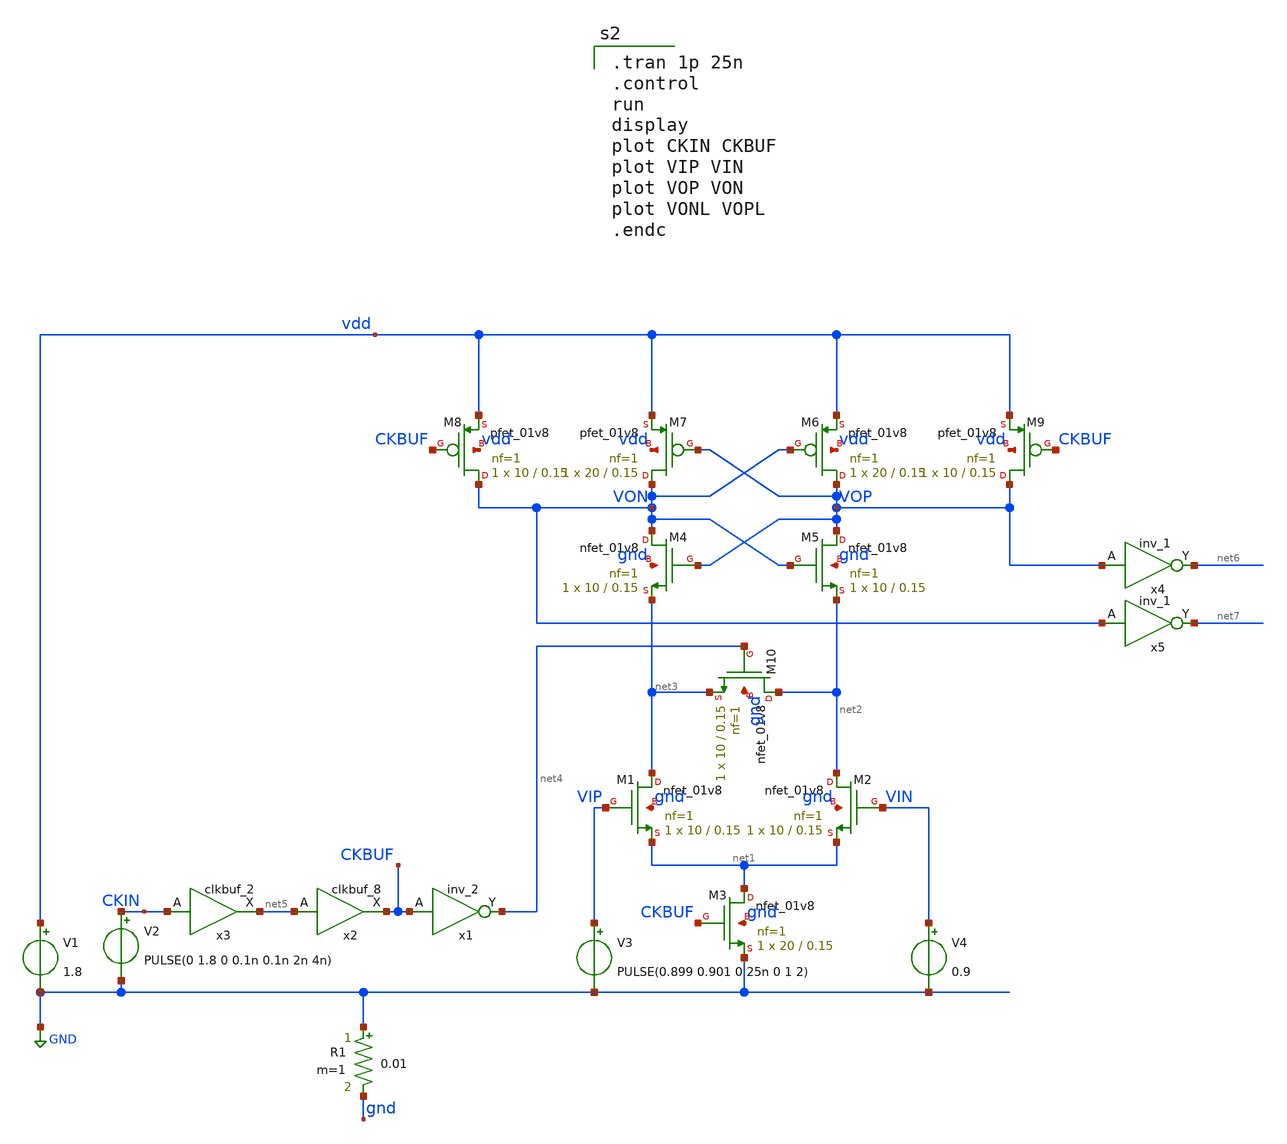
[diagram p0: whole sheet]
** sch_path: xschem/adc_strongarm.sch
**.subckt adc_strongarm
XM1 net3 VIP net1 gnd sky130_fd_pr__nfet_01v8 L=0.15 W=10 nf=1 ad='int((nf+1)/2) * W/nf * 0.29' as='int((nf+2)/2) * W/nf * 0.29'
+ pd='2*int((nf+1)/2) * (W/nf + 0.29)' ps='2*int((nf+2)/2) * (W/nf + 0.29)' nrd='0.29 / W' nrs='0.29 / W'
+ sa=0 sb=0 sd=0 mult=1 m=1
XM2 net2 VIN net1 gnd sky130_fd_pr__nfet_01v8 L=0.15 W=10 nf=1 ad='int((nf+1)/2) * W/nf * 0.29' as='int((nf+2)/2) * W/nf * 0.29'
+ pd='2*int((nf+1)/2) * (W/nf + 0.29)' ps='2*int((nf+2)/2) * (W/nf + 0.29)' nrd='0.29 / W' nrs='0.29 / W'
+ sa=0 sb=0 sd=0 mult=1 m=1
XM3 net1 CKBUF GND gnd sky130_fd_pr__nfet_01v8 L=0.15 W=20 nf=1 ad='int((nf+1)/2) * W/nf * 0.29' as='int((nf+2)/2) * W/nf * 0.29'
+ pd='2*int((nf+1)/2) * (W/nf + 0.29)' ps='2*int((nf+2)/2) * (W/nf + 0.29)' nrd='0.29 / W' nrs='0.29 / W'
+ sa=0 sb=0 sd=0 mult=1 m=1
XM4 VON VOP net3 gnd sky130_fd_pr__nfet_01v8 L=0.15 W=10 nf=1 ad='int((nf+1)/2) * W/nf * 0.29' as='int((nf+2)/2) * W/nf * 0.29'
+ pd='2*int((nf+1)/2) * (W/nf + 0.29)' ps='2*int((nf+2)/2) * (W/nf + 0.29)' nrd='0.29 / W' nrs='0.29 / W'
+ sa=0 sb=0 sd=0 mult=1 m=1
XM5 VOP VON net2 gnd sky130_fd_pr__nfet_01v8 L=0.15 W=10 nf=1 ad='int((nf+1)/2) * W/nf * 0.29' as='int((nf+2)/2) * W/nf * 0.29'
+ pd='2*int((nf+1)/2) * (W/nf + 0.29)' ps='2*int((nf+2)/2) * (W/nf + 0.29)' nrd='0.29 / W' nrs='0.29 / W'
+ sa=0 sb=0 sd=0 mult=1 m=1
XM6 VOP VON vdd vdd sky130_fd_pr__pfet_01v8 L=0.15 W=20 nf=1 ad='int((nf+1)/2) * W/nf * 0.29' as='int((nf+2)/2) * W/nf * 0.29'
+ pd='2*int((nf+1)/2) * (W/nf + 0.29)' ps='2*int((nf+2)/2) * (W/nf + 0.29)' nrd='0.29 / W' nrs='0.29 / W'
+ sa=0 sb=0 sd=0 mult=1 m=1
XM7 VON VOP vdd vdd sky130_fd_pr__pfet_01v8 L=0.15 W=20 nf=1 ad='int((nf+1)/2) * W/nf * 0.29' as='int((nf+2)/2) * W/nf * 0.29'
+ pd='2*int((nf+1)/2) * (W/nf + 0.29)' ps='2*int((nf+2)/2) * (W/nf + 0.29)' nrd='0.29 / W' nrs='0.29 / W'
+ sa=0 sb=0 sd=0 mult=1 m=1
XM8 VON CKBUF vdd vdd sky130_fd_pr__pfet_01v8 L=0.15 W=10 nf=1 ad='int((nf+1)/2) * W/nf * 0.29' as='int((nf+2)/2) * W/nf * 0.29'
+ pd='2*int((nf+1)/2) * (W/nf + 0.29)' ps='2*int((nf+2)/2) * (W/nf + 0.29)' nrd='0.29 / W' nrs='0.29 / W'
+ sa=0 sb=0 sd=0 mult=1 m=1
XM9 VOP CKBUF vdd vdd sky130_fd_pr__pfet_01v8 L=0.15 W=10 nf=1 ad='int((nf+1)/2) * W/nf * 0.29' as='int((nf+2)/2) * W/nf * 0.29'
+ pd='2*int((nf+1)/2) * (W/nf + 0.29)' ps='2*int((nf+2)/2) * (W/nf + 0.29)' nrd='0.29 / W' nrs='0.29 / W'
+ sa=0 sb=0 sd=0 mult=1 m=1
V1 vdd GND 1.8
x1 CKBUF gnd gnd vdd vdd net4 sky130_fd_sc_hd__inv_2
XM10 net2 net4 net3 gnd sky130_fd_pr__nfet_01v8 L=0.15 W=10 nf=1 ad='int((nf+1)/2) * W/nf * 0.29' as='int((nf+2)/2) * W/nf * 0.29'
+ pd='2*int((nf+1)/2) * (W/nf + 0.29)' ps='2*int((nf+2)/2) * (W/nf + 0.29)' nrd='0.29 / W' nrs='0.29 / W'
+ sa=0 sb=0 sd=0 mult=1 m=1
x2 net5 gnd gnd vdd vdd CKBUF sky130_fd_sc_hd__clkbuf_8
V2 CKIN GND PULSE(0 1.8 0 0.1n 0.1n 2n 4n)
V3 VIP GND PULSE(0.899 0.901 0 25n 0 1 2)
V4 VIN GND 0.9
R1 GND gnd 0.01 m=1
x3 CKIN gnd gnd vdd vdd net5 sky130_fd_sc_hd__clkbuf_2
x4 VOP gnd gnd vdd vdd net6 sky130_fd_sc_hd__inv_1
x5 VON gnd gnd vdd vdd net7 sky130_fd_sc_hd__inv_1
**** begin user architecture code
.lib $::SKYWATER_MODELS/sky130.lib.spice tt
.include /home/al/openmpw/pdk_1/sky130B/libs.ref/sky130_fd_sc_hd/spice/sky130_fd_sc_hd.spice


.tran 1p 25n
.control
run
display
plot CKIN CKBUF
plot VIP VIN
plot VOP VON
plot VONL VOPL
.endc


**** end user architecture code
**.ends
.GLOBAL GND
.end
